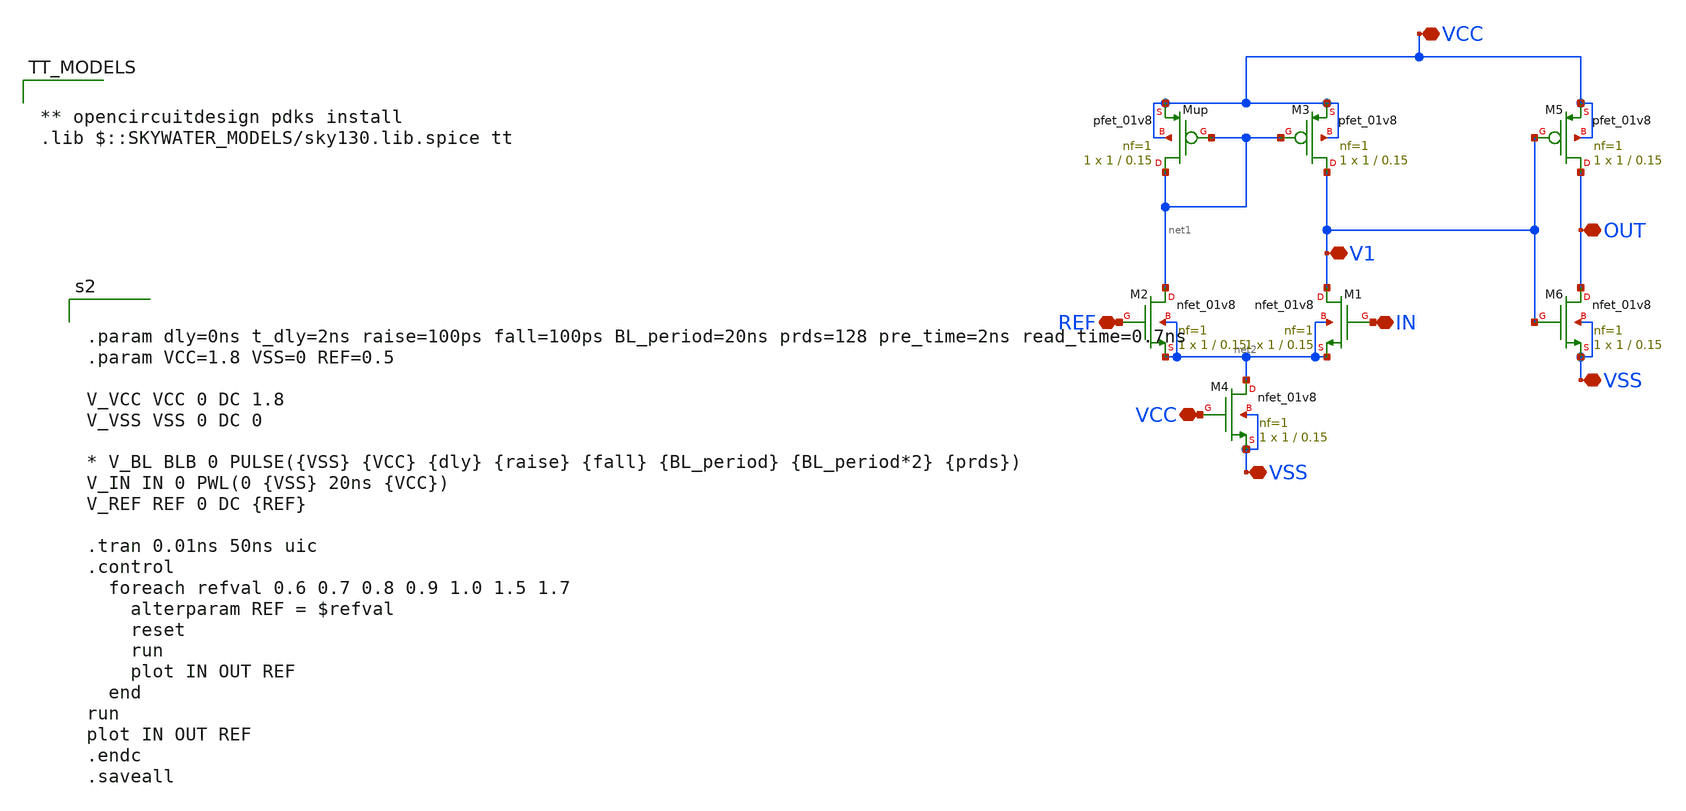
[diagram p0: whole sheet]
** sch_path: voltage_comp/voltage_comp.sch
**.subckt voltage_comp VSS VCC REF IN VCC OUT V1 VSS
*.iopin VSS
*.iopin VCC
*.iopin REF
*.iopin IN
*.iopin VCC
*.iopin OUT
*.iopin V1
*.iopin VSS
XM2 net1 REF net2 net2 sky130_fd_pr__nfet_01v8 L=0.15 W=1 nf=1 ad='int((1 + 1)/2) * 1 / 1 * 0.29' as='int((1 + 2)/2) * 1 / 1 * 0.29'
+ pd='2*int((1 + 1)/2) * (1 / 1 + 0.29)' ps='2*int((1 + 2)/2) * (1 / 1 + 0.29)' nrd='0.29 / 1 ' nrs='0.29 / 1 '
+ sa=0 sb=0 sd=0 mult=1 m=1
XMup net1 net1 VCC VCC sky130_fd_pr__pfet_01v8 L=0.15 W=1 nf=1 ad='int((1 + 1)/2) * 1 / 1 * 0.29' as='int((1 + 2)/2) * 1 / 1 * 0.29'
+ pd='2*int((1 + 1)/2) * (1 / 1 + 0.29)' ps='2*int((1 + 2)/2) * (1 / 1 + 0.29)' nrd='0.29 / 1 ' nrs='0.29 / 1 '
+ sa=0 sb=0 sd=0 mult=1 m=1
XM1 V1 IN net2 net2 sky130_fd_pr__nfet_01v8 L=0.15 W=1 nf=1 ad='int((1 + 1)/2) * 1 / 1 * 0.29' as='int((1 + 2)/2) * 1 / 1 * 0.29'
+ pd='2*int((1 + 1)/2) * (1 / 1 + 0.29)' ps='2*int((1 + 2)/2) * (1 / 1 + 0.29)' nrd='0.29 / 1 ' nrs='0.29 / 1 '
+ sa=0 sb=0 sd=0 mult=1 m=1
XM3 V1 net1 VCC VCC sky130_fd_pr__pfet_01v8 L=0.15 W=1 nf=1 ad='int((1 + 1)/2) * 1 / 1 * 0.29' as='int((1 + 2)/2) * 1 / 1 * 0.29'
+ pd='2*int((1 + 1)/2) * (1 / 1 + 0.29)' ps='2*int((1 + 2)/2) * (1 / 1 + 0.29)' nrd='0.29 / 1 ' nrs='0.29 / 1 '
+ sa=0 sb=0 sd=0 mult=1 m=1
XM4 net2 VCC VSS VSS sky130_fd_pr__nfet_01v8 L=0.15 W=1 nf=1 ad='int((1 + 1)/2) * 1 / 1 * 0.29' as='int((1 + 2)/2) * 1 / 1 * 0.29'
+ pd='2*int((1 + 1)/2) * (1 / 1 + 0.29)' ps='2*int((1 + 2)/2) * (1 / 1 + 0.29)' nrd='0.29 / 1 ' nrs='0.29 / 1 '
+ sa=0 sb=0 sd=0 mult=1 m=1
XM5 OUT V1 VCC VCC sky130_fd_pr__pfet_01v8 L=0.15 W=1 nf=1 ad='int((1 + 1)/2) * 1 / 1 * 0.29' as='int((1 + 2)/2) * 1 / 1 * 0.29'
+ pd='2*int((1 + 1)/2) * (1 / 1 + 0.29)' ps='2*int((1 + 2)/2) * (1 / 1 + 0.29)' nrd='0.29 / 1 ' nrs='0.29 / 1 '
+ sa=0 sb=0 sd=0 mult=1 m=1
XM6 OUT V1 VSS VSS sky130_fd_pr__nfet_01v8 L=0.15 W=1 nf=1 ad='int((1 + 1)/2) * 1 / 1 * 0.29' as='int((1 + 2)/2) * 1 / 1 * 0.29'
+ pd='2*int((1 + 1)/2) * (1 / 1 + 0.29)' ps='2*int((1 + 2)/2) * (1 / 1 + 0.29)' nrd='0.29 / 1 ' nrs='0.29 / 1 '
+ sa=0 sb=0 sd=0 mult=1 m=1
**** begin user architecture code


.param dly=0ns t_dly=2ns raise=100ps fall=100ps BL_period=20ns prds=128 pre_time=2ns read_time=0.7ns
.param VCC=1.8 VSS=0 REF=0.5

V_VCC VCC 0 DC 1.8
V_VSS VSS 0 DC 0

* V_BL BLB 0 PULSE({VSS} {VCC} {dly} {raise} {fall} {BL_period} {BL_period*2} {prds})
V_IN IN 0 PWL(0 {VSS} 20ns {VCC})
V_REF REF 0 DC {REF}

.tran 0.01ns 50ns uic
.control
  foreach refval 0.6 0.7 0.8 0.9 1.0 1.5 1.7
    alterparam REF = $refval
    reset
    run
    plot IN OUT REF
  end
run
plot IN OUT REF
.endc
.saveall




** opencircuitdesign pdks install
.lib $::SKYWATER_MODELS/sky130.lib.spice tt

**** end user architecture code
**.ends
.end
